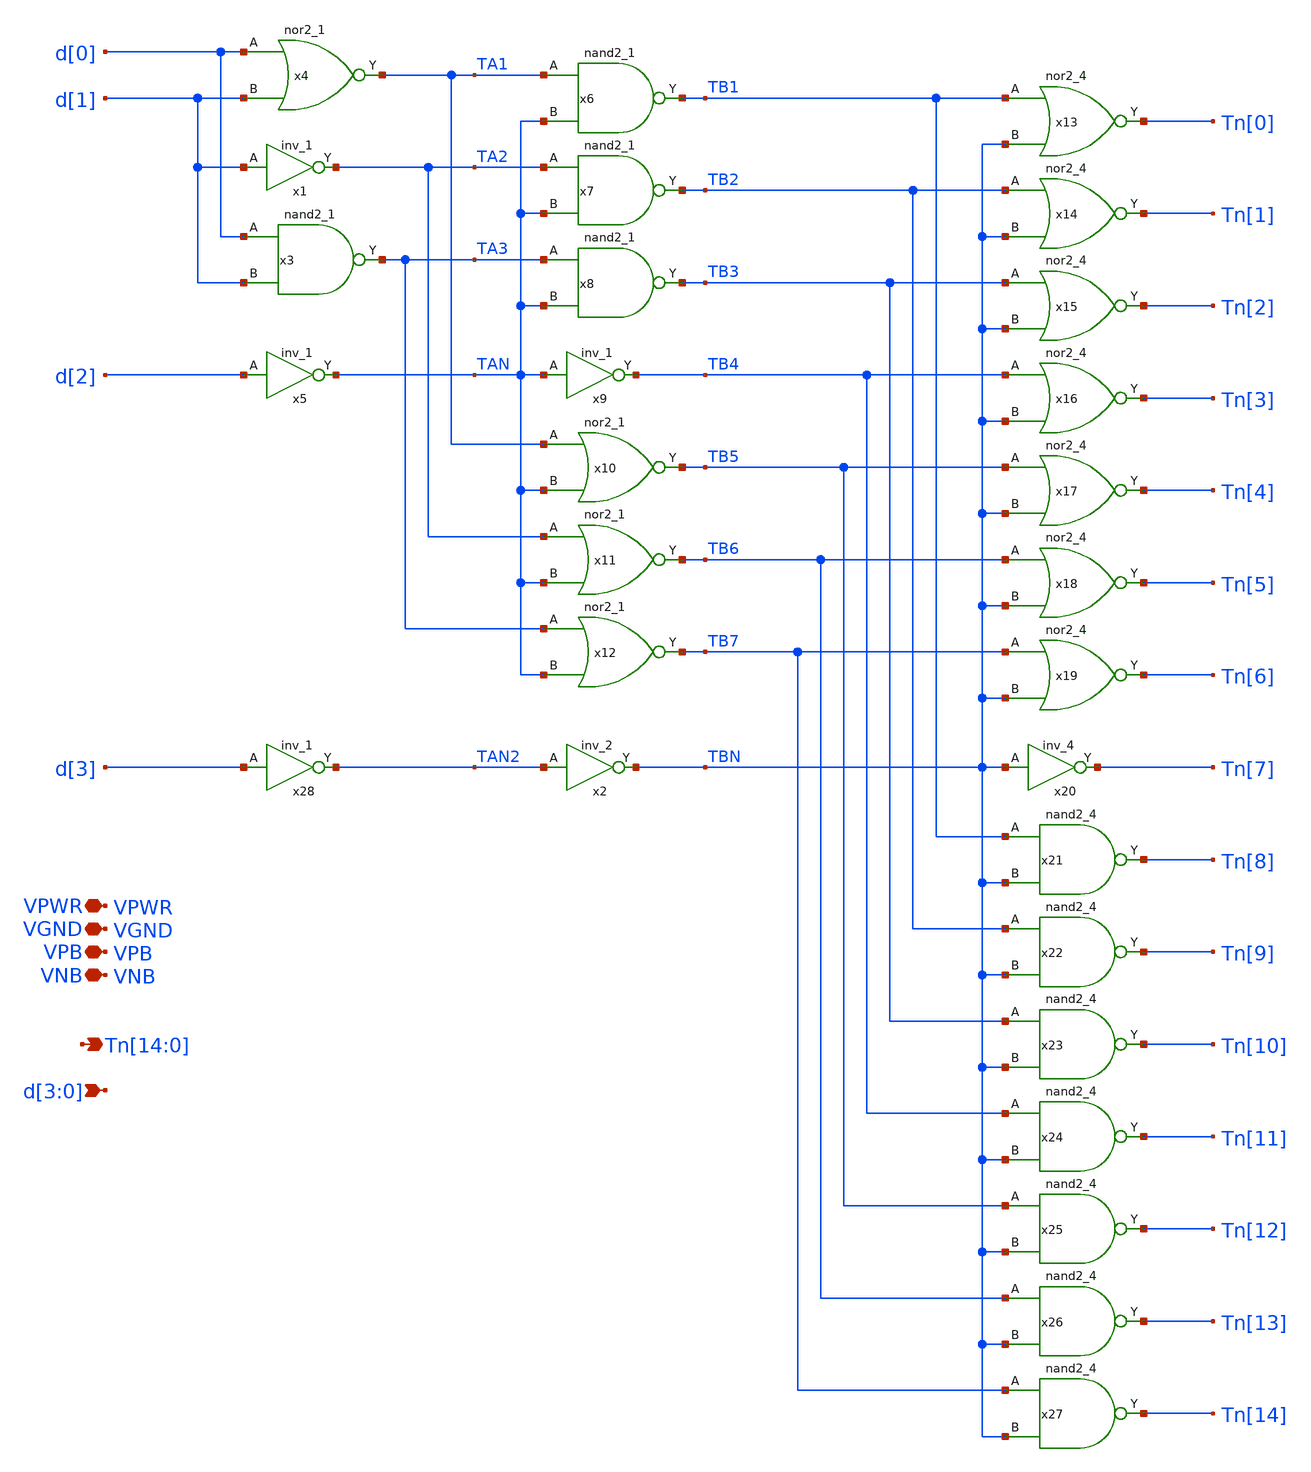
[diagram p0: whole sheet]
** sch_path: xschem/thermo15.sch
**.subckt thermo15 VPWR d[3],d[2],d[1],d[0] VGND VPB VNB
*+ Tn[14],Tn[13],Tn[12],Tn[11],Tn[10],Tn[9],Tn[8],Tn[7],Tn[6],Tn[5],Tn[4],Tn[3],Tn[2],Tn[1],Tn[0]
*.iopin VPWR
*.ipin d[3],d[2],d[1],d[0]
*.iopin VGND
*.iopin VPB
*.iopin VNB
*.opin
*+ Tn[14],Tn[13],Tn[12],Tn[11],Tn[10],Tn[9],Tn[8],Tn[7],Tn[6],Tn[5],Tn[4],Tn[3],Tn[2],Tn[1],Tn[0]
x1 d[1] VGND VNB VPB VPWR TA2 sky130_fd_sc_hd__inv_1
x2 TAN2 VGND VNB VPB VPWR TBN sky130_fd_sc_hd__inv_2
x3 d[0] d[1] VGND VNB VPB VPWR TA3 sky130_fd_sc_hd__nand2_1
x4 d[0] d[1] VGND VNB VPB VPWR TA1 sky130_fd_sc_hd__nor2_1
x5 d[2] VGND VNB VPB VPWR TAN sky130_fd_sc_hd__inv_1
x6 TA1 TAN VGND VNB VPB VPWR TB1 sky130_fd_sc_hd__nand2_1
x7 TA2 TAN VGND VNB VPB VPWR TB2 sky130_fd_sc_hd__nand2_1
x8 TA3 TAN VGND VNB VPB VPWR TB3 sky130_fd_sc_hd__nand2_1
x9 TAN VGND VNB VPB VPWR TB4 sky130_fd_sc_hd__inv_1
x10 TA1 TAN VGND VNB VPB VPWR TB5 sky130_fd_sc_hd__nor2_1
x11 TA2 TAN VGND VNB VPB VPWR TB6 sky130_fd_sc_hd__nor2_1
x12 TA3 TAN VGND VNB VPB VPWR TB7 sky130_fd_sc_hd__nor2_1
x13 TB1 TBN VGND VNB VPB VPWR Tn[0] sky130_fd_sc_hd__nor2_4
x14 TB2 TBN VGND VNB VPB VPWR Tn[1] sky130_fd_sc_hd__nor2_4
x15 TB3 TBN VGND VNB VPB VPWR Tn[2] sky130_fd_sc_hd__nor2_4
x16 TB4 TBN VGND VNB VPB VPWR Tn[3] sky130_fd_sc_hd__nor2_4
x17 TB5 TBN VGND VNB VPB VPWR Tn[4] sky130_fd_sc_hd__nor2_4
x18 TB6 TBN VGND VNB VPB VPWR Tn[5] sky130_fd_sc_hd__nor2_4
x19 TB7 TBN VGND VNB VPB VPWR Tn[6] sky130_fd_sc_hd__nor2_4
x20 TBN VGND VNB VPB VPWR Tn[7] sky130_fd_sc_hd__inv_4
x21 TB1 TBN VGND VNB VPB VPWR Tn[8] sky130_fd_sc_hd__nand2_4
x22 TB2 TBN VGND VNB VPB VPWR Tn[9] sky130_fd_sc_hd__nand2_4
x23 TB3 TBN VGND VNB VPB VPWR Tn[10] sky130_fd_sc_hd__nand2_4
x24 TB4 TBN VGND VNB VPB VPWR Tn[11] sky130_fd_sc_hd__nand2_4
x25 TB5 TBN VGND VNB VPB VPWR Tn[12] sky130_fd_sc_hd__nand2_4
x26 TB6 TBN VGND VNB VPB VPWR Tn[13] sky130_fd_sc_hd__nand2_4
x27 TB7 TBN VGND VNB VPB VPWR Tn[14] sky130_fd_sc_hd__nand2_4
x28 d[3] VGND VNB VPB VPWR TAN2 sky130_fd_sc_hd__inv_1
**.ends
.end
